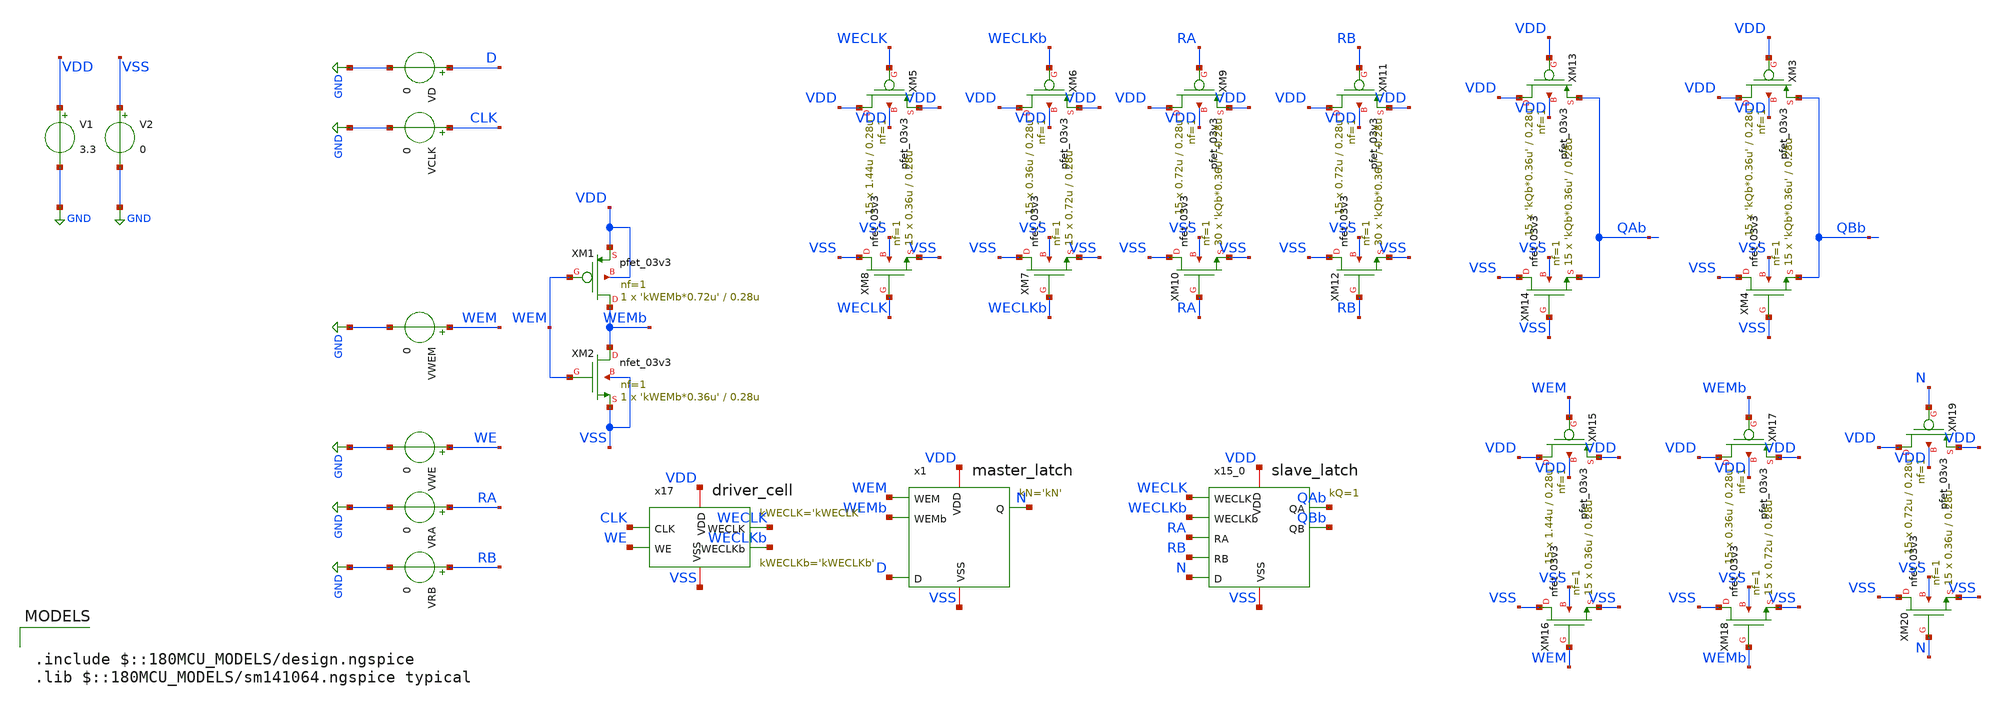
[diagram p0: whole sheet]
** sch_path: CAD3/rf_sizing_tb.sch
**.subckt rf_sizing_tb
XM1 WEMb WEM VDD VDD pfet_03v3 L=0.28u W='kWEMb*0.72u' nf=1 ad='int((nf+1)/2) * W/nf * 0.18u' as='int((nf+2)/2) * W/nf * 0.18u'
+ pd='2*int((nf+1)/2) * (W/nf + 0.18u)' ps='2*int((nf+2)/2) * (W/nf + 0.18u)' nrd='0.18u / W' nrs='0.18u / W'
+ sa=0 sb=0 sd=0 m=1
XM2 WEMb WEM VSS VSS nfet_03v3 L=0.28u W='kWEMb*0.36u' nf=1 ad='int((nf+1)/2) * W/nf * 0.18u' as='int((nf+2)/2) * W/nf * 0.18u'
+ pd='2*int((nf+1)/2) * (W/nf + 0.18u)' ps='2*int((nf+2)/2) * (W/nf + 0.18u)' nrd='0.18u / W' nrs='0.18u / W'
+ sa=0 sb=0 sd=0 m=1
x15_0 VDD VSS QAb WECLK WECLKb RA RB QBb N slave_latch kQ=1
x1 VDD VSS N WEM WEMb D master_latch kN='kN'
x17 CLK WE WECLKb VDD VSS WECLK driver_cell kWECLK='kWECLK' kWECLKb='kWECLKb'
XM13 VDD VDD QAb VDD pfet_03v3 L=0.28u W='kQb*0.36u' nf=1 ad='int((nf+1)/2) * W/nf * 0.18u' as='int((nf+2)/2) * W/nf * 0.18u'
+ pd='2*int((nf+1)/2) * (W/nf + 0.18u)' ps='2*int((nf+2)/2) * (W/nf + 0.18u)' nrd='0.18u / W' nrs='0.18u / W'
+ sa=0 sb=0 sd=0 m=15
XM14 VSS VSS QAb VSS nfet_03v3 L=0.28u W='kQb*0.36u' nf=1 ad='int((nf+1)/2) * W/nf * 0.18u' as='int((nf+2)/2) * W/nf * 0.18u'
+ pd='2*int((nf+1)/2) * (W/nf + 0.18u)' ps='2*int((nf+2)/2) * (W/nf + 0.18u)' nrd='0.18u / W' nrs='0.18u / W'
+ sa=0 sb=0 sd=0 m=15
XM3 VDD VDD QBb VDD pfet_03v3 L=0.28u W='kQb*0.36u' nf=1 ad='int((nf+1)/2) * W/nf * 0.18u' as='int((nf+2)/2) * W/nf * 0.18u'
+ pd='2*int((nf+1)/2) * (W/nf + 0.18u)' ps='2*int((nf+2)/2) * (W/nf + 0.18u)' nrd='0.18u / W' nrs='0.18u / W'
+ sa=0 sb=0 sd=0 m=15
XM4 VSS VSS QBb VSS nfet_03v3 L=0.28u W='kQb*0.36u' nf=1 ad='int((nf+1)/2) * W/nf * 0.18u' as='int((nf+2)/2) * W/nf * 0.18u'
+ pd='2*int((nf+1)/2) * (W/nf + 0.18u)' ps='2*int((nf+2)/2) * (W/nf + 0.18u)' nrd='0.18u / W' nrs='0.18u / W'
+ sa=0 sb=0 sd=0 m=15
XM5 VDD WECLK VDD VDD pfet_03v3 L=0.28u W=1.44u nf=1 ad='int((nf+1)/2) * W/nf * 0.18u' as='int((nf+2)/2) * W/nf * 0.18u'
+ pd='2*int((nf+1)/2) * (W/nf + 0.18u)' ps='2*int((nf+2)/2) * (W/nf + 0.18u)' nrd='0.18u / W' nrs='0.18u / W'
+ sa=0 sb=0 sd=0 m=15
XM8 VSS WECLK VSS VSS nfet_03v3 L=0.28u W=0.36u nf=1 ad='int((nf+1)/2) * W/nf * 0.18u' as='int((nf+2)/2) * W/nf * 0.18u'
+ pd='2*int((nf+1)/2) * (W/nf + 0.18u)' ps='2*int((nf+2)/2) * (W/nf + 0.18u)' nrd='0.18u / W' nrs='0.18u / W'
+ sa=0 sb=0 sd=0 m=15
XM6 VDD WECLKb VDD VDD pfet_03v3 L=0.28u W=0.36u nf=1 ad='int((nf+1)/2) * W/nf * 0.18u' as='int((nf+2)/2) * W/nf * 0.18u'
+ pd='2*int((nf+1)/2) * (W/nf + 0.18u)' ps='2*int((nf+2)/2) * (W/nf + 0.18u)' nrd='0.18u / W' nrs='0.18u / W'
+ sa=0 sb=0 sd=0 m=15
XM7 VSS WECLKb VSS VSS nfet_03v3 L=0.28u W=0.72u nf=1 ad='int((nf+1)/2) * W/nf * 0.18u' as='int((nf+2)/2) * W/nf * 0.18u'
+ pd='2*int((nf+1)/2) * (W/nf + 0.18u)' ps='2*int((nf+2)/2) * (W/nf + 0.18u)' nrd='0.18u / W' nrs='0.18u / W'
+ sa=0 sb=0 sd=0 m=15
XM9 VDD RA VDD VDD pfet_03v3 L=0.28u W=0.72u nf=1 ad='int((nf+1)/2) * W/nf * 0.18u' as='int((nf+2)/2) * W/nf * 0.18u'
+ pd='2*int((nf+1)/2) * (W/nf + 0.18u)' ps='2*int((nf+2)/2) * (W/nf + 0.18u)' nrd='0.18u / W' nrs='0.18u / W'
+ sa=0 sb=0 sd=0 m=15
XM10 VSS RA VSS VSS nfet_03v3 L=0.28u W='kQb*0.36u' nf=1 ad='int((nf+1)/2) * W/nf * 0.18u' as='int((nf+2)/2) * W/nf * 0.18u'
+ pd='2*int((nf+1)/2) * (W/nf + 0.18u)' ps='2*int((nf+2)/2) * (W/nf + 0.18u)' nrd='0.18u / W' nrs='0.18u / W'
+ sa=0 sb=0 sd=0 m=30
XM11 VDD RB VDD VDD pfet_03v3 L=0.28u W=0.72u nf=1 ad='int((nf+1)/2) * W/nf * 0.18u' as='int((nf+2)/2) * W/nf * 0.18u'
+ pd='2*int((nf+1)/2) * (W/nf + 0.18u)' ps='2*int((nf+2)/2) * (W/nf + 0.18u)' nrd='0.18u / W' nrs='0.18u / W'
+ sa=0 sb=0 sd=0 m=15
XM12 VSS RB VSS VSS nfet_03v3 L=0.28u W='kQb*0.36u' nf=1 ad='int((nf+1)/2) * W/nf * 0.18u' as='int((nf+2)/2) * W/nf * 0.18u'
+ pd='2*int((nf+1)/2) * (W/nf + 0.18u)' ps='2*int((nf+2)/2) * (W/nf + 0.18u)' nrd='0.18u / W' nrs='0.18u / W'
+ sa=0 sb=0 sd=0 m=30
XM15 VDD WEM VDD VDD pfet_03v3 L=0.28u W=1.44u nf=1 ad='int((nf+1)/2) * W/nf * 0.18u' as='int((nf+2)/2) * W/nf * 0.18u'
+ pd='2*int((nf+1)/2) * (W/nf + 0.18u)' ps='2*int((nf+2)/2) * (W/nf + 0.18u)' nrd='0.18u / W' nrs='0.18u / W'
+ sa=0 sb=0 sd=0 m=15
XM16 VSS WEM VSS VSS nfet_03v3 L=0.28u W=0.36u nf=1 ad='int((nf+1)/2) * W/nf * 0.18u' as='int((nf+2)/2) * W/nf * 0.18u'
+ pd='2*int((nf+1)/2) * (W/nf + 0.18u)' ps='2*int((nf+2)/2) * (W/nf + 0.18u)' nrd='0.18u / W' nrs='0.18u / W'
+ sa=0 sb=0 sd=0 m=15
XM17 VDD WEMb VDD VDD pfet_03v3 L=0.28u W=0.36u nf=1 ad='int((nf+1)/2) * W/nf * 0.18u' as='int((nf+2)/2) * W/nf * 0.18u'
+ pd='2*int((nf+1)/2) * (W/nf + 0.18u)' ps='2*int((nf+2)/2) * (W/nf + 0.18u)' nrd='0.18u / W' nrs='0.18u / W'
+ sa=0 sb=0 sd=0 m=15
XM18 VSS WEMb VSS VSS nfet_03v3 L=0.28u W=0.72u nf=1 ad='int((nf+1)/2) * W/nf * 0.18u' as='int((nf+2)/2) * W/nf * 0.18u'
+ pd='2*int((nf+1)/2) * (W/nf + 0.18u)' ps='2*int((nf+2)/2) * (W/nf + 0.18u)' nrd='0.18u / W' nrs='0.18u / W'
+ sa=0 sb=0 sd=0 m=15
XM19 VDD N VDD VDD pfet_03v3 L=0.28u W=0.72u nf=1 ad='int((nf+1)/2) * W/nf * 0.18u' as='int((nf+2)/2) * W/nf * 0.18u'
+ pd='2*int((nf+1)/2) * (W/nf + 0.18u)' ps='2*int((nf+2)/2) * (W/nf + 0.18u)' nrd='0.18u / W' nrs='0.18u / W'
+ sa=0 sb=0 sd=0 m=15
XM20 VSS N VSS VSS nfet_03v3 L=0.28u W=0.36u nf=1 ad='int((nf+1)/2) * W/nf * 0.18u' as='int((nf+2)/2) * W/nf * 0.18u'
+ pd='2*int((nf+1)/2) * (W/nf + 0.18u)' ps='2*int((nf+2)/2) * (W/nf + 0.18u)' nrd='0.18u / W' nrs='0.18u / W'
+ sa=0 sb=0 sd=0 m=15
V1 VDD GND 3.3
V2 VSS GND 0
VD D GND 0
VCLK CLK GND 0
VWEM WEM GND 0
VWE WE GND 0
VRA RA GND 0
VRB RB GND 0
**** begin user architecture code


** kWECLK SWEEP

.param kWECLKb=5.27
.param kWECLK=1
.param kWEMb=1
.param kQb=1
.param kN=1

.control

** Define input signals
let f = 1e8
let T = 1/f
let PW = T/2
let INF = 5 * T

let tstop = 2 * T
let tstep = 0.001 * T
let NTRIALS = 100

compose kVALS start=4.5 stop=6 lin=$&NTRIALS
compose TRISE start=0 stop=0 lin=$&NTRIALS
compose TFALL start=0 stop=0 lin=$&NTRIALS

let idx = 0
while idx < NTRIALS
	let kVAL = kVALS[idx]
	alterparam kWECLK = $&kVAL
	reset

	** Enable WE
	alter @VWE[DC] = 3.3

	** Test pulses
	alter @VCLK[PWL] = [ 0 0 $&PW 0 $&PW 3.3 $&T 3.3 $&T 0 ]

	tran $&tstep $&tstop
	meas tran TPLH TRIG V(CLK) VAL=1.65 RISE=1 TARG V(WECLK) VAL=1.65 FALL=1
	meas tran TPHL TRIG V(CLK) VAL=1.65 FALL=1 TARG V(WECLK) VAL=1.65 RISE=1
	let TRISE[idx] = $&TPLH
	let TFALL[idx] = $&TPHL
	let idx = idx + 1
end

plot TRISE vs kVALS
plot TFALL vs kVALS

let minval = minimum(TRISE)
let idxR = 0
while TRISE[idxR] > minval
  let idxR = idxR + 1
end
print kVALS[idxR]

let minval = minimum(TFALL)
let idxF = 0
while TFALL[idxF] > minval
  let idxF = idxF + 1
end
print kVALS[idxF]

.endc



.include $::180MCU_MODELS/design.ngspice
.lib $::180MCU_MODELS/sm141064.ngspice typical

**** end user architecture code
**.ends

* expanding   symbol:  engn1600-team1/CAD3/slave_latch.sym # of pins=9
** sym_path: CAD3/slave_latch.sym
** sch_path: CAD3/slave_latch.sch
.subckt slave_latch VDD VSS QA WECLK WECLKb RA RB QB D  kQ=1
*.ipin D
*.ipin RA
*.ipin RB
*.ipin WECLKb
*.ipin WECLK
*.opin QA
*.opin QB
*.iopin VDD
*.iopin VSS
XM1 net1 WECLKb net2 VDD pfet_03v3 L=0.28u W=0.22u nf=1 ad='int((nf+1)/2) * W/nf * 0.18u' as='int((nf+2)/2) * W/nf * 0.18u'
+ pd='2*int((nf+1)/2) * (W/nf + 0.18u)' ps='2*int((nf+2)/2) * (W/nf + 0.18u)' nrd='0.18u / W' nrs='0.18u / W'
+ sa=0 sb=0 sd=0 m=1
XM2 net1 D VDD VDD pfet_03v3 L=0.28u W=0.22u nf=1 ad='int((nf+1)/2) * W/nf * 0.18u' as='int((nf+2)/2) * W/nf * 0.18u'
+ pd='2*int((nf+1)/2) * (W/nf + 0.18u)' ps='2*int((nf+2)/2) * (W/nf + 0.18u)' nrd='0.18u / W' nrs='0.18u / W'
+ sa=0 sb=0 sd=0 m=1
XM3 net3 net2 VDD VDD pfet_03v3 L=0.28u W=0.22u nf=1 ad='int((nf+1)/2) * W/nf * 0.18u' as='int((nf+2)/2) * W/nf * 0.18u'
+ pd='2*int((nf+1)/2) * (W/nf + 0.18u)' ps='2*int((nf+2)/2) * (W/nf + 0.18u)' nrd='0.18u / W' nrs='0.18u / W'
+ sa=0 sb=0 sd=0 m=1
XM4 net4 net2 VDD VDD pfet_03v3 L=0.28u W=0.22u nf=1 ad='int((nf+1)/2) * W/nf * 0.18u' as='int((nf+2)/2) * W/nf * 0.18u'
+ pd='2*int((nf+1)/2) * (W/nf + 0.18u)' ps='2*int((nf+2)/2) * (W/nf + 0.18u)' nrd='0.18u / W' nrs='0.18u / W'
+ sa=0 sb=0 sd=0 m=1
XM5 VDD WECLK net8 VDD pfet_03v3 L=0.28u W=0.22u nf=1 ad='int((nf+1)/2) * W/nf * 0.18u' as='int((nf+2)/2) * W/nf * 0.18u'
+ pd='2*int((nf+1)/2) * (W/nf + 0.18u)' ps='2*int((nf+2)/2) * (W/nf + 0.18u)' nrd='0.18u / W' nrs='0.18u / W'
+ sa=0 sb=0 sd=0 m=1
XM6 net8 net4 net2 VDD pfet_03v3 L=0.28u W=0.22u nf=1 ad='int((nf+1)/2) * W/nf * 0.18u' as='int((nf+2)/2) * W/nf * 0.18u'
+ pd='2*int((nf+1)/2) * (W/nf + 0.18u)' ps='2*int((nf+2)/2) * (W/nf + 0.18u)' nrd='0.18u / W' nrs='0.18u / W'
+ sa=0 sb=0 sd=0 m=1
XM7 net1 D VSS VSS nfet_03v3 L=0.28u W=0.22u nf=1 ad='int((nf+1)/2) * W/nf * 0.18u' as='int((nf+2)/2) * W/nf * 0.18u'
+ pd='2*int((nf+1)/2) * (W/nf + 0.18u)' ps='2*int((nf+2)/2) * (W/nf + 0.18u)' nrd='0.18u / W' nrs='0.18u / W'
+ sa=0 sb=0 sd=0 m=1
XM8 net1 WECLK net2 VSS nfet_03v3 L=0.28u W=0.22u nf=1 ad='int((nf+1)/2) * W/nf * 0.18u' as='int((nf+2)/2) * W/nf * 0.18u'
+ pd='2*int((nf+1)/2) * (W/nf + 0.18u)' ps='2*int((nf+2)/2) * (W/nf + 0.18u)' nrd='0.18u / W' nrs='0.18u / W'
+ sa=0 sb=0 sd=0 m=1
XM9 net3 net2 VSS VSS nfet_03v3 L=0.28u W=0.22u nf=1 ad='int((nf+1)/2) * W/nf * 0.18u' as='int((nf+2)/2) * W/nf * 0.18u'
+ pd='2*int((nf+1)/2) * (W/nf + 0.18u)' ps='2*int((nf+2)/2) * (W/nf + 0.18u)' nrd='0.18u / W' nrs='0.18u / W'
+ sa=0 sb=0 sd=0 m=1
XM10 net4 net2 VSS VSS nfet_03v3 L=0.28u W=0.22u nf=1 ad='int((nf+1)/2) * W/nf * 0.18u' as='int((nf+2)/2) * W/nf * 0.18u'
+ pd='2*int((nf+1)/2) * (W/nf + 0.18u)' ps='2*int((nf+2)/2) * (W/nf + 0.18u)' nrd='0.18u / W' nrs='0.18u / W'
+ sa=0 sb=0 sd=0 m=1
XM11 net7 net4 net2 VSS nfet_03v3 L=0.28u W=0.22u nf=1 ad='int((nf+1)/2) * W/nf * 0.18u' as='int((nf+2)/2) * W/nf * 0.18u'
+ pd='2*int((nf+1)/2) * (W/nf + 0.18u)' ps='2*int((nf+2)/2) * (W/nf + 0.18u)' nrd='0.18u / W' nrs='0.18u / W'
+ sa=0 sb=0 sd=0 m=1
XM12 VSS WECLKb net7 VSS nfet_03v3 L=0.28u W=0.22u nf=1 ad='int((nf+1)/2) * W/nf * 0.18u' as='int((nf+2)/2) * W/nf * 0.18u'
+ pd='2*int((nf+1)/2) * (W/nf + 0.18u)' ps='2*int((nf+2)/2) * (W/nf + 0.18u)' nrd='0.18u / W' nrs='0.18u / W'
+ sa=0 sb=0 sd=0 m=1
XM13 net3 net5 QB VDD pfet_03v3 L=0.28u W=0.22u nf=1 ad='int((nf+1)/2) * W/nf * 0.18u' as='int((nf+2)/2) * W/nf * 0.18u'
+ pd='2*int((nf+1)/2) * (W/nf + 0.18u)' ps='2*int((nf+2)/2) * (W/nf + 0.18u)' nrd='0.18u / W' nrs='0.18u / W'
+ sa=0 sb=0 sd=0 m=1
XM14 net3 RB QB VSS nfet_03v3 L=0.28u W=0.22u nf=1 ad='int((nf+1)/2) * W/nf * 0.18u' as='int((nf+2)/2) * W/nf * 0.18u'
+ pd='2*int((nf+1)/2) * (W/nf + 0.18u)' ps='2*int((nf+2)/2) * (W/nf + 0.18u)' nrd='0.18u / W' nrs='0.18u / W'
+ sa=0 sb=0 sd=0 m=1
XM15 net5 RB VDD VDD pfet_03v3 L=0.28u W=0.22u nf=1 ad='int((nf+1)/2) * W/nf * 0.18u' as='int((nf+2)/2) * W/nf * 0.18u'
+ pd='2*int((nf+1)/2) * (W/nf + 0.18u)' ps='2*int((nf+2)/2) * (W/nf + 0.18u)' nrd='0.18u / W' nrs='0.18u / W'
+ sa=0 sb=0 sd=0 m=1
XM16 net5 RB VSS VSS nfet_03v3 L=0.28u W=0.22u nf=1 ad='int((nf+1)/2) * W/nf * 0.18u' as='int((nf+2)/2) * W/nf * 0.18u'
+ pd='2*int((nf+1)/2) * (W/nf + 0.18u)' ps='2*int((nf+2)/2) * (W/nf + 0.18u)' nrd='0.18u / W' nrs='0.18u / W'
+ sa=0 sb=0 sd=0 m=1
XM21 net3 net6 QA VDD pfet_03v3 L=0.28u W=0.22u nf=1 ad='int((nf+1)/2) * W/nf * 0.18u' as='int((nf+2)/2) * W/nf * 0.18u'
+ pd='2*int((nf+1)/2) * (W/nf + 0.18u)' ps='2*int((nf+2)/2) * (W/nf + 0.18u)' nrd='0.18u / W' nrs='0.18u / W'
+ sa=0 sb=0 sd=0 m=1
XM22 net3 RA QA VSS nfet_03v3 L=0.28u W=0.22u nf=1 ad='int((nf+1)/2) * W/nf * 0.18u' as='int((nf+2)/2) * W/nf * 0.18u'
+ pd='2*int((nf+1)/2) * (W/nf + 0.18u)' ps='2*int((nf+2)/2) * (W/nf + 0.18u)' nrd='0.18u / W' nrs='0.18u / W'
+ sa=0 sb=0 sd=0 m=1
XM23 net6 RA VDD VDD pfet_03v3 L=0.28u W=0.22u nf=1 ad='int((nf+1)/2) * W/nf * 0.18u' as='int((nf+2)/2) * W/nf * 0.18u'
+ pd='2*int((nf+1)/2) * (W/nf + 0.18u)' ps='2*int((nf+2)/2) * (W/nf + 0.18u)' nrd='0.18u / W' nrs='0.18u / W'
+ sa=0 sb=0 sd=0 m=1
XM24 net6 RA VSS VSS nfet_03v3 L=0.28u W=0.22u nf=1 ad='int((nf+1)/2) * W/nf * 0.18u' as='int((nf+2)/2) * W/nf * 0.18u'
+ pd='2*int((nf+1)/2) * (W/nf + 0.18u)' ps='2*int((nf+2)/2) * (W/nf + 0.18u)' nrd='0.18u / W' nrs='0.18u / W'
+ sa=0 sb=0 sd=0 m=1
.ends


* expanding   symbol:  engn1600-team1/CAD3/master_latch.sym # of pins=6
** sym_path: CAD3/master_latch.sym
** sch_path: CAD3/master_latch.sch
.subckt master_latch VDD VSS Q WEM WEMb D  kN=1
*.ipin D
*.ipin WEMb
*.ipin WEM
*.iopin VSS
*.iopin VDD
*.opin Q
XM3 net1 WEMb net2 VDD pfet_03v3 L=0.28u W=0.36u nf=1 ad='int((nf+1)/2) * W/nf * 0.18u' as='int((nf+2)/2) * W/nf * 0.18u'
+ pd='2*int((nf+1)/2) * (W/nf + 0.18u)' ps='2*int((nf+2)/2) * (W/nf + 0.18u)' nrd='0.18u / W' nrs='0.18u / W'
+ sa=0 sb=0 sd=0 m=1
XM7 net1 D VDD VDD pfet_03v3 L=0.28u W=0.72u nf=1 ad='int((nf+1)/2) * W/nf * 0.18u' as='int((nf+2)/2) * W/nf * 0.18u'
+ pd='2*int((nf+1)/2) * (W/nf + 0.18u)' ps='2*int((nf+2)/2) * (W/nf + 0.18u)' nrd='0.18u / W' nrs='0.18u / W'
+ sa=0 sb=0 sd=0 m=1
XM8 Q net2 VDD VDD pfet_03v3 L=0.28u W=0.72u nf=4 ad='int((nf+1)/2) * W/nf * 0.18u' as='int((nf+2)/2) * W/nf * 0.18u'
+ pd='2*int((nf+1)/2) * (W/nf + 0.18u)' ps='2*int((nf+2)/2) * (W/nf + 0.18u)' nrd='0.18u / W' nrs='0.18u / W'
+ sa=0 sb=0 sd=0 m=1
XM9 net3 net2 VDD VDD pfet_03v3 L=0.28u W=0.36u nf=1 ad='int((nf+1)/2) * W/nf * 0.18u' as='int((nf+2)/2) * W/nf * 0.18u'
+ pd='2*int((nf+1)/2) * (W/nf + 0.18u)' ps='2*int((nf+2)/2) * (W/nf + 0.18u)' nrd='0.18u / W' nrs='0.18u / W'
+ sa=0 sb=0 sd=0 m=1
XM10 VDD WEM net5 VDD pfet_03v3 L=0.28u W=0.36u nf=1 ad='int((nf+1)/2) * W/nf * 0.18u' as='int((nf+2)/2) * W/nf * 0.18u'
+ pd='2*int((nf+1)/2) * (W/nf + 0.18u)' ps='2*int((nf+2)/2) * (W/nf + 0.18u)' nrd='0.18u / W' nrs='0.18u / W'
+ sa=0 sb=0 sd=0 m=1
XM12 net5 net3 net2 VDD pfet_03v3 L=0.28u W=0.36u nf=1 ad='int((nf+1)/2) * W/nf * 0.18u' as='int((nf+2)/2) * W/nf * 0.18u'
+ pd='2*int((nf+1)/2) * (W/nf + 0.18u)' ps='2*int((nf+2)/2) * (W/nf + 0.18u)' nrd='0.18u / W' nrs='0.18u / W'
+ sa=0 sb=0 sd=0 m=1
XM19 net1 D VSS VSS nfet_03v3 L=0.28u W=0.36u nf=1 ad='int((nf+1)/2) * W/nf * 0.18u' as='int((nf+2)/2) * W/nf * 0.18u'
+ pd='2*int((nf+1)/2) * (W/nf + 0.18u)' ps='2*int((nf+2)/2) * (W/nf + 0.18u)' nrd='0.18u / W' nrs='0.18u / W'
+ sa=0 sb=0 sd=0 m=1
XM20 net1 WEM net2 VSS nfet_03v3 L=0.28u W=0.36u nf=1 ad='int((nf+1)/2) * W/nf * 0.18u' as='int((nf+2)/2) * W/nf * 0.18u'
+ pd='2*int((nf+1)/2) * (W/nf + 0.18u)' ps='2*int((nf+2)/2) * (W/nf + 0.18u)' nrd='0.18u / W' nrs='0.18u / W'
+ sa=0 sb=0 sd=0 m=1
XM21 Q net2 VSS VSS nfet_03v3 L=0.28u W=0.36u nf=4 ad='int((nf+1)/2) * W/nf * 0.18u' as='int((nf+2)/2) * W/nf * 0.18u'
+ pd='2*int((nf+1)/2) * (W/nf + 0.18u)' ps='2*int((nf+2)/2) * (W/nf + 0.18u)' nrd='0.18u / W' nrs='0.18u / W'
+ sa=0 sb=0 sd=0 m=1
XM22 net3 net2 VSS VSS nfet_03v3 L=0.28u W=0.36u nf=1 ad='int((nf+1)/2) * W/nf * 0.18u' as='int((nf+2)/2) * W/nf * 0.18u'
+ pd='2*int((nf+1)/2) * (W/nf + 0.18u)' ps='2*int((nf+2)/2) * (W/nf + 0.18u)' nrd='0.18u / W' nrs='0.18u / W'
+ sa=0 sb=0 sd=0 m=1
XM23 net4 net3 net2 VSS nfet_03v3 L=0.28u W=0.36u nf=1 ad='int((nf+1)/2) * W/nf * 0.18u' as='int((nf+2)/2) * W/nf * 0.18u'
+ pd='2*int((nf+1)/2) * (W/nf + 0.18u)' ps='2*int((nf+2)/2) * (W/nf + 0.18u)' nrd='0.18u / W' nrs='0.18u / W'
+ sa=0 sb=0 sd=0 m=1
XM24 VSS WEMb net4 VSS nfet_03v3 L=0.28u W=0.36u nf=1 ad='int((nf+1)/2) * W/nf * 0.18u' as='int((nf+2)/2) * W/nf * 0.18u'
+ pd='2*int((nf+1)/2) * (W/nf + 0.18u)' ps='2*int((nf+2)/2) * (W/nf + 0.18u)' nrd='0.18u / W' nrs='0.18u / W'
+ sa=0 sb=0 sd=0 m=1
.ends


* expanding   symbol:  engn1600-team1/CAD3/driver_cell.sym # of pins=6
** sym_path: CAD3/driver_cell.sym
** sch_path: CAD3/driver_cell.sch
.subckt driver_cell CLK WE WECLKb VDD VSS WECLK  kWECLK=1 kWECLKb=1
*.ipin CLK
*.ipin WE
*.iopin VSS
*.iopin VDD
*.opin WECLKb
*.opin WECLK
XM13 WECLK net1 VDD VDD pfet_03v3 L=0.28u W=2.54u nf=1 ad='int((nf+1)/2) * W/nf * 0.18u' as='int((nf+2)/2) * W/nf * 0.18u'
+ pd='2*int((nf+1)/2) * (W/nf + 0.18u)' ps='2*int((nf+2)/2) * (W/nf + 0.18u)' nrd='0.18u / W' nrs='0.18u / W'
+ sa=0 sb=0 sd=0 m=1
XM14 WECLK net1 VSS VSS nfet_03v3 L=0.28u W=1.27u nf=1 ad='int((nf+1)/2) * W/nf * 0.18u' as='int((nf+2)/2) * W/nf * 0.18u'
+ pd='2*int((nf+1)/2) * (W/nf + 0.18u)' ps='2*int((nf+2)/2) * (W/nf + 0.18u)' nrd='0.18u / W' nrs='0.18u / W'
+ sa=0 sb=0 sd=0 m=1
XM1 WECLKb WECLK VDD VDD pfet_03v3 L=0.28u W=2.68u nf=1 ad='int((nf+1)/2) * W/nf * 0.18u' as='int((nf+2)/2) * W/nf * 0.18u'
+ pd='2*int((nf+1)/2) * (W/nf + 0.18u)' ps='2*int((nf+2)/2) * (W/nf + 0.18u)' nrd='0.18u / W' nrs='0.18u / W'
+ sa=0 sb=0 sd=0 m=1
XM2 WECLKb WECLK VSS VSS nfet_03v3 L=0.28u W=1.34u nf=1 ad='int((nf+1)/2) * W/nf * 0.18u' as='int((nf+2)/2) * W/nf * 0.18u'
+ pd='2*int((nf+1)/2) * (W/nf + 0.18u)' ps='2*int((nf+2)/2) * (W/nf + 0.18u)' nrd='0.18u / W' nrs='0.18u / W'
+ sa=0 sb=0 sd=0 m=1
XM3 net1 CLK VDD VDD pfet_03v3 L=0.28u W=0.72u nf=1 ad='int((nf+1)/2) * W/nf * 0.18u' as='int((nf+2)/2) * W/nf * 0.18u'
+ pd='2*int((nf+1)/2) * (W/nf + 0.18u)' ps='2*int((nf+2)/2) * (W/nf + 0.18u)' nrd='0.18u / W' nrs='0.18u / W'
+ sa=0 sb=0 sd=0 m=1
XM4 net1 WE VDD VDD pfet_03v3 L=0.28u W=0.72u nf=1 ad='int((nf+1)/2) * W/nf * 0.18u' as='int((nf+2)/2) * W/nf * 0.18u'
+ pd='2*int((nf+1)/2) * (W/nf + 0.18u)' ps='2*int((nf+2)/2) * (W/nf + 0.18u)' nrd='0.18u / W' nrs='0.18u / W'
+ sa=0 sb=0 sd=0 m=1
XM5 net2 WE VSS VSS nfet_03v3 L=0.28u W=0.72u nf=1 ad='int((nf+1)/2) * W/nf * 0.18u' as='int((nf+2)/2) * W/nf * 0.18u'
+ pd='2*int((nf+1)/2) * (W/nf + 0.18u)' ps='2*int((nf+2)/2) * (W/nf + 0.18u)' nrd='0.18u / W' nrs='0.18u / W'
+ sa=0 sb=0 sd=0 m=1
XM6 net1 CLK net2 VSS nfet_03v3 L=0.28u W=0.72u nf=1 ad='int((nf+1)/2) * W/nf * 0.18u' as='int((nf+2)/2) * W/nf * 0.18u'
+ pd='2*int((nf+1)/2) * (W/nf + 0.18u)' ps='2*int((nf+2)/2) * (W/nf + 0.18u)' nrd='0.18u / W' nrs='0.18u / W'
+ sa=0 sb=0 sd=0 m=1
.ends

.GLOBAL GND
.end
